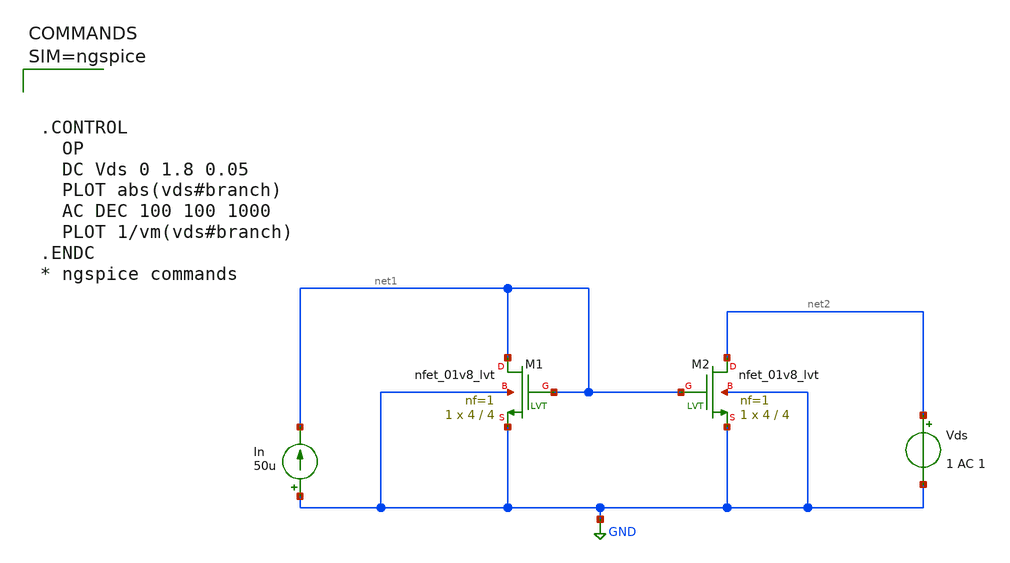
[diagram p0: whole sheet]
** sch_path: xschem/currentmirrnmos2.sch
**.subckt currentmirrnmos2
XM1 net1 net1 GND GND sky130_fd_pr__nfet_01v8_lvt L=4 W=4 nf=1 ad='int((1 + 1)/2) * 4 / 1 * 0.29' as='int((1 + 2)/2) * 4 / 1 * 0.29'
+ pd='2*int((1 + 1)/2) * (4 / 1 + 0.29)' ps='2*int((1 + 2)/2) * (4 / 1 + 0.29)' nrd='0.29 / 4 ' nrs='0.29 / 4 '
+ sa=0 sb=0 sd=0 mult=1 m=1
In GND net1 50u
Vds net2 GND 1 AC 1
XM2 net2 net1 GND GND sky130_fd_pr__nfet_01v8_lvt L=4 W=4 nf=1 ad='int((1 + 1)/2) * 4 / 1 * 0.29' as='int((1 + 2)/2) * 4 / 1 * 0.29'
+ pd='2*int((1 + 1)/2) * (4 / 1 + 0.29)' ps='2*int((1 + 2)/2) * (4 / 1 + 0.29)' nrd='0.29 / 4 ' nrs='0.29 / 4 '
+ sa=0 sb=0 sd=0 mult=1 m=1
**** begin user architecture code

** opencircuitdesign pdks install
.lib $::SKYWATER_MODELS/sky130.lib.spice tt





.CONTROL
  OP
  DC Vds 0 1.8 0.05
  PLOT abs(vds#branch)
  AC DEC 100 100 1000
  PLOT 1/vm(vds#branch)
.ENDC
* ngspice commands



**** end user architecture code
**.ends
.GLOBAL GND
.end
